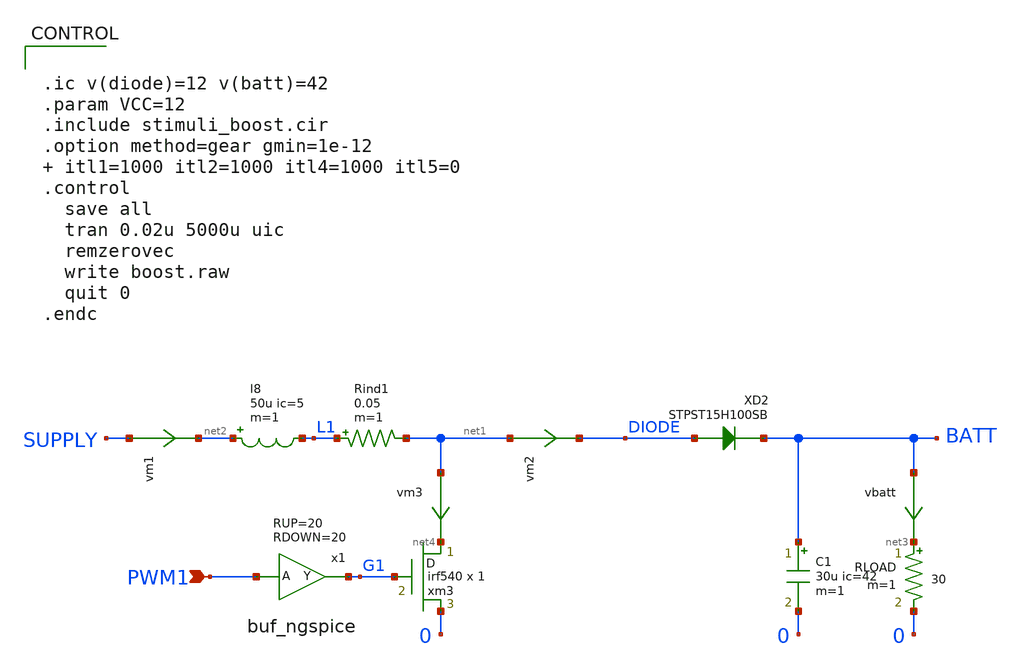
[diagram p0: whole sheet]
** sch_path: xschem_library/ngspice/boost.sch
* xschem_library/ngspice/buf_ngspice.sym:
* Copyright (C) 1998-2024 Stefan Frederik Schippers
* This program is free software; you can redistribute it and/or modify
* it under the terms of the GNU General Public License as published by
* the Free Software Foundation; either version 2 of the License, or
* (at your option) any later version.
**.subckt boost PWM1
*.ipin PWM1
RLOAD net3 0 30 m=1
C1 BATT 0 30u ic=42 m=1
vbatt BATT net3 0
.save i(vbatt)
vm2 net1 DIODE 0
.save i(vm2)
vm1 SUPPLY net2 0
.save i(vm1)
XD2 DIODE BATT STPST15H100SB
xm3 net4 G1 0 irf540 m=1
l8 net2 L1 50u ic=5 m=1
Rind1 L1 net1 0.05 m=1
vm3 net1 net4 0
.save i(vm3)
x1 G1 PWM1 buf_ngspice RUP=20 RDOWN=20
**.ends

* expanding   symbol:  buf_ngspice.sym # of pins=2
** sym_path: xschem_library/ngspice/buf_ngspice.sym
** sch_path: xschem_library/ngspice/buf_ngspice.sch
.subckt buf_ngspice Y A  RUP=2000 RDOWN=1000
*.ipin A
*.opin Y
B1 net1 0 V = 'VCC/2*(1+tanh((V(A1)-VCC/2)*100))'
R1 Y1 net1 ROUT m=1
C3 Y1 0 8f m=1
C1 A1 0 4f m=1
V1 Y Y1 0
V2 A1 A 0
.ends

**** begin user architecture code


.ic v(diode)=12 v(batt)=42
.param VCC=12
.include stimuli_boost.cir
.option method=gear gmin=1e-12  itl1=1000 itl2=1000 itl4=1000 itl5=0
.control
  save all
  tran 0.02u 5000u uic
  remzerovec
  write boost.raw
  quit 0
.endc



*******************************************************************
* Model name       : STPST15H100SB
* Description      : 100 V - 15 A power Schottky trench diode
* Package type     : DPAK
*******************************************************************
*model STPST15H100SB  anode
*                     | cathode
*                     | |
*                     | |
.subckt STPST15H100SB 1 2
r1 1 13 0.1E-3
r2 1 13 0.1E-3
d1 13 2 dx
.model dx       D(IS=383.61E-9 N=1.0502 RS=10.043E-3 IKF=3.9178 CJO=2.0881E-9 M=1.0083  VJ=5.1229
+ ISR=262.18E-9 TT=0 EG=.69 XTI=2 FC=0.5)
.ends


.SUBCKT irf540 1 2 3
M1 9 7 8 8 MM L=100u W=100u
* Default values used in MM:
* The voltage-dependent capacitances are
* not included. Other default values are:
* RS=0 RD=0 LD=0 CBD=0 CBS=0 CGBO=0
.MODEL MM NMOS LEVEL=1 IS=1e-32 VTO=3.56362 LAMBDA=0.00291031 KP=25.0081 CGSO=1.60584e-05
+ CGDO=4.25919e-07
RS 8 3 0.0317085
D1 3 1 MD
.MODEL MD D IS=1.02194e-10 RS=0.00968022 N=1.21527 BV=100 IBV=0.00025 EG=1.2 XTI=3.03885 TT=1e-07
+ CJO=1.81859e-09 VJ=1.1279 M=0.449161 FC=0.5
RDS 3 1 4e+06
RD 9 1 0.0135649
RG 2 7 5.11362
D2 4 5 MD1
* Default values used in MD1:
* RS=0 EG=1.11 XTI=3.0 TT=0
* BV=infinite IBV=1mA
.MODEL MD1 D IS=1e-32 N=50 CJO=2.49697e-09 VJ=0.5 M=0.9 FC=1e-08
D3 0 5 MD2
* Default values used in MD2:
* EG=1.11 XTI=3.0 TT=0 CJO=0
* BV=infinite IBV=1mA
.MODEL MD2 D IS=1e-10 N=0.4 RS=3e-06
RL 5 10 1
FI2 7 9 VFI2 -1
VFI2 4 0 0
EV16 10 0 9 7 1
CAP 11 10 2.49697e-09
FI1 7 9 VFI1 -1
VFI1 11 6 0
RCAP 6 10 1
D4 0 6 MD3
* Default values used in MD3:
* EG=1.11 XTI=3.0 TT=0 CJO=0
* RS=0 BV=infinite IBV=1mA
.MODEL MD3 D IS=1e-10 N=0.4
.ENDS

**** end user architecture code
.end
